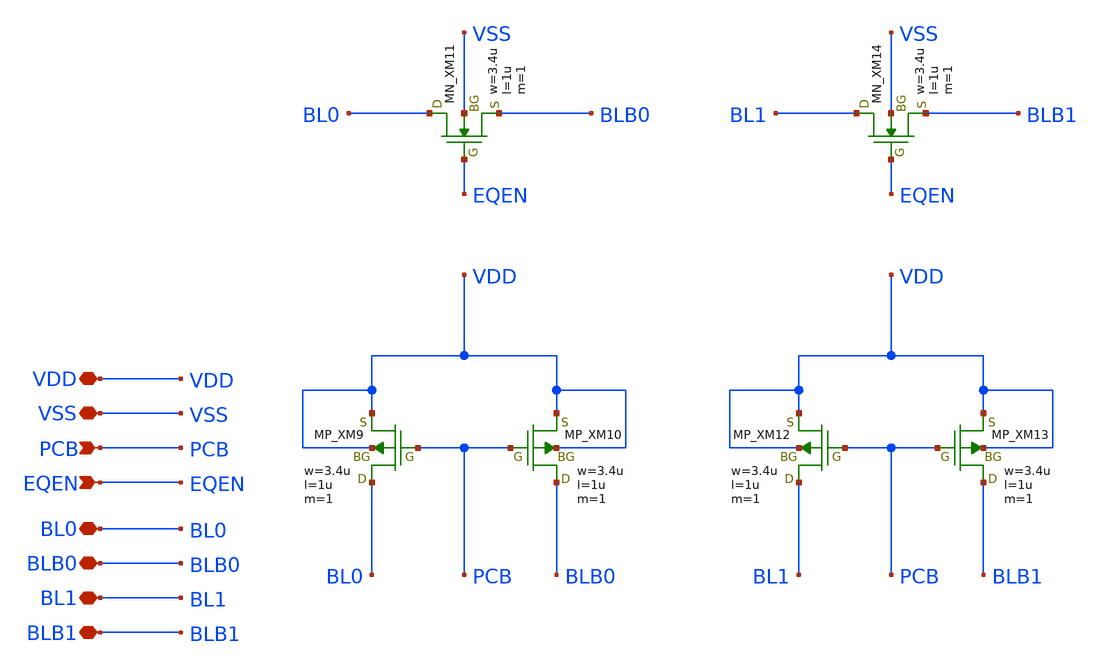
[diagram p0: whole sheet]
** sch_path: array/2word_x_8bit/precharge.sch
**.subckt precharge VDD VSS PCB EQEN BL0 BLB0 BL1 BLB1
*.iopin VDD
*.iopin VSS
*.ipin PCB
*.ipin EQEN
*.iopin BL0
*.iopin BLB0
*.iopin BL1
*.iopin BLB1
XXM9 BL0 PCB VDD VDD PMOS w=3.4u l=1u nrd=0 nrs=0 m=1
XXM10 BLB0 PCB VDD VDD PMOS w=3.4u l=1u nrd=0 nrs=0 m=1
XXM11 BL0 EQEN BLB0 VSS NMOS w=3.4u l=1u nrd=0 nrs=0 m=1
XXM12 BL1 PCB VDD VDD PMOS w=3.4u l=1u nrd=0 nrs=0 m=1
XXM13 BLB1 PCB VDD VDD PMOS w=3.4u l=1u nrd=0 nrs=0 m=1
XXM14 BL1 EQEN BLB1 VSS NMOS w=3.4u l=1u nrd=0 nrs=0 m=1
**.ends
.end
